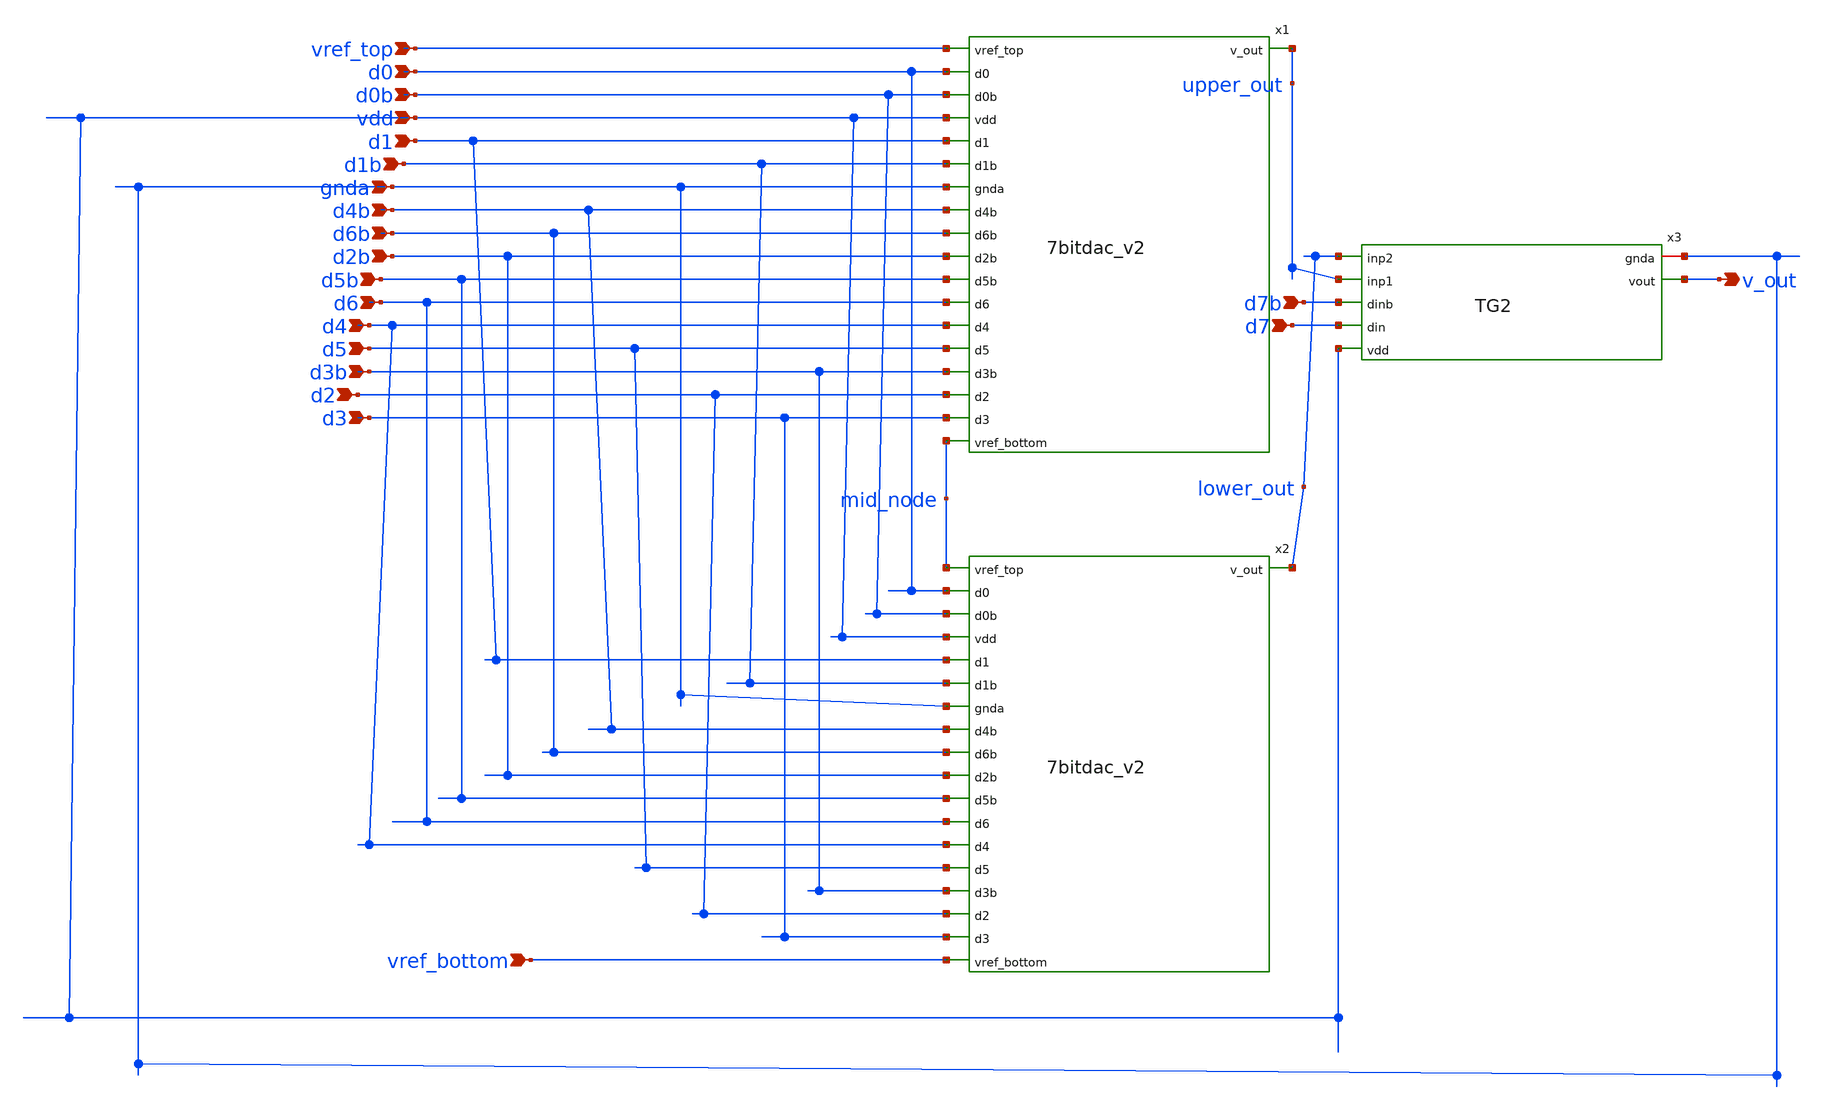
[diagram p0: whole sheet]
** sch_path: prelayout/8bitdac_v2.sch
**.subckt 8bitdac_v2 vref_top d0 d0b vdd d1 d1b gnda d4b d6b d2b d5b d6 d4 d5 d3b d3 d2 d7b d7 v_out
*+ vref_bottom
*.ipin vref_top
*.ipin d0
*.ipin d0b
*.ipin vdd
*.ipin d1
*.ipin d1b
*.ipin gnda
*.ipin d4b
*.ipin d6b
*.ipin d2b
*.ipin d5b
*.ipin d6
*.ipin d4
*.ipin d5
*.ipin d3b
*.ipin d3
*.ipin d2
*.ipin d7b
*.ipin d7
*.opin v_out
*.ipin vref_bottom
x1 vref_top d0 d0b vdd d1 d1b gnda upper_out d4b d6b d2b d5b d6 d4 d5 d3b d2 d3 mid_node 7bitdac_v2
x2 mid_node d0 d0b vdd d1 d1b gnda lower_out d4b d6b d2b d5b d6 d4 d5 d3b d2 d3 vref_bottom
+ 7bitdac_v2
Xx3 gnda v_out lower_out upper_out d7b d7 vdd TG2
**.ends
.end
